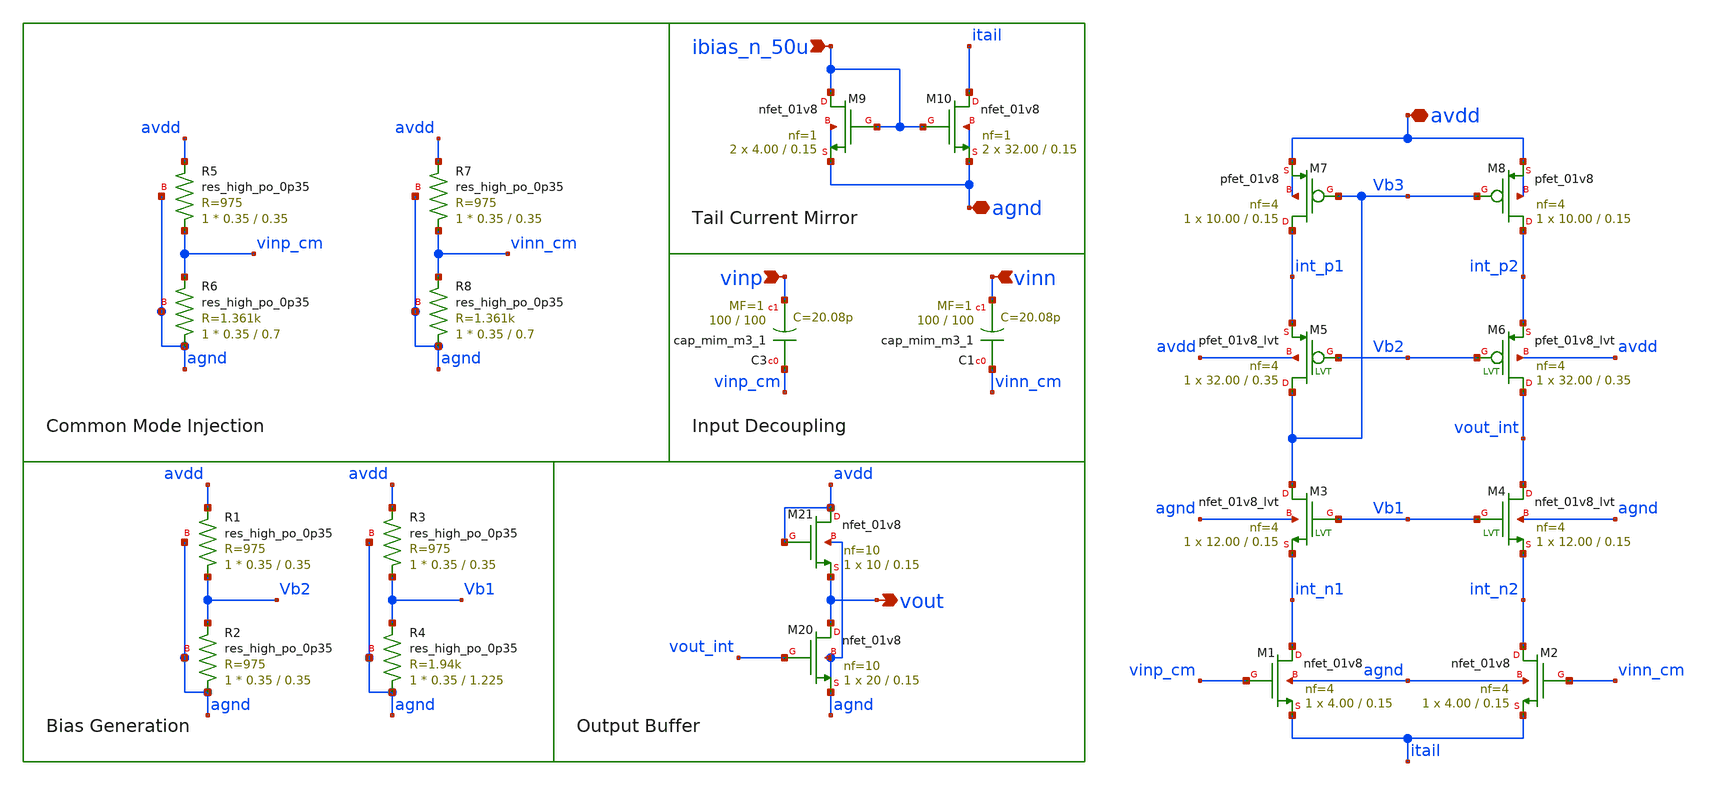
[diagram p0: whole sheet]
** sch_path: AMP/Final_Cascode_Simplfied.sch
**.subckt Final_Cascode_Simplfied avdd vinp vout agnd vinn ibias_n_50u
*.iopin avdd
*.ipin vinp
*.opin vout
*.iopin agnd
*.ipin vinn
*.ipin ibias_n_50u
XM1 int_n1 vinp_cm itail agnd sky130_fd_pr__nfet_01v8 L=0.15 W=4.00 nf=4 ad='int((nf+1)/2) * W/nf * 0.29'
+ as='int((nf+2)/2) * W/nf * 0.29' pd='2*int((nf+1)/2) * (W/nf + 0.29)' ps='2*int((nf+2)/2) * (W/nf + 0.29)'
+ nrd='0.29 / W' nrs='0.29 / W' sa=0 sb=0 sd=0 mult=1 m=1
XM2 int_n2 vinn_cm itail agnd sky130_fd_pr__nfet_01v8 L=0.15 W=4.00 nf=4 ad='int((nf+1)/2) * W/nf * 0.29'
+ as='int((nf+2)/2) * W/nf * 0.29' pd='2*int((nf+1)/2) * (W/nf + 0.29)' ps='2*int((nf+2)/2) * (W/nf + 0.29)'
+ nrd='0.29 / W' nrs='0.29 / W' sa=0 sb=0 sd=0 mult=1 m=1
XM7 int_p1 Vb3 avdd avdd sky130_fd_pr__pfet_01v8 L=0.15 W=10.00 nf=4 ad='int((nf+1)/2) * W/nf * 0.29'
+ as='int((nf+2)/2) * W/nf * 0.29' pd='2*int((nf+1)/2) * (W/nf + 0.29)' ps='2*int((nf+2)/2) * (W/nf + 0.29)'
+ nrd='0.29 / W' nrs='0.29 / W' sa=0 sb=0 sd=0 mult=1 m=1
XM8 int_p2 Vb3 avdd avdd sky130_fd_pr__pfet_01v8 L=0.15 W=10.00 nf=4 ad='int((nf+1)/2) * W/nf * 0.29'
+ as='int((nf+2)/2) * W/nf * 0.29' pd='2*int((nf+1)/2) * (W/nf + 0.29)' ps='2*int((nf+2)/2) * (W/nf + 0.29)'
+ nrd='0.29 / W' nrs='0.29 / W' sa=0 sb=0 sd=0 mult=1 m=1
XM9 ibias_n_50u ibias_n_50u agnd agnd sky130_fd_pr__nfet_01v8 L=0.15 W=4.00 nf=1 ad='int((nf+1)/2) * W/nf * 0.29'
+ as='int((nf+2)/2) * W/nf * 0.29' pd='2*int((nf+1)/2) * (W/nf + 0.29)' ps='2*int((nf+2)/2) * (W/nf + 0.29)'
+ nrd='0.29 / W' nrs='0.29 / W' sa=0 sb=0 sd=0 mult=2 m=2
XM10 itail ibias_n_50u agnd agnd sky130_fd_pr__nfet_01v8 L=0.15 W=32.00 nf=1 ad='int((nf+1)/2) * W/nf * 0.29'
+ as='int((nf+2)/2) * W/nf * 0.29' pd='2*int((nf+1)/2) * (W/nf + 0.29)' ps='2*int((nf+2)/2) * (W/nf + 0.29)'
+ nrd='0.29 / W' nrs='0.29 / W' sa=0 sb=0 sd=0 mult=2 m=2
XM3 Vb3 Vb1 int_n1 agnd sky130_fd_pr__nfet_01v8_lvt L=0.15 W=12.00 nf=4 ad='int((nf+1)/2) * W/nf * 0.29'
+ as='int((nf+2)/2) * W/nf * 0.29' pd='2*int((nf+1)/2) * (W/nf + 0.29)' ps='2*int((nf+2)/2) * (W/nf + 0.29)'
+ nrd='0.29 / W' nrs='0.29 / W' sa=0 sb=0 sd=0 mult=1 m=1
XM4 vout_int Vb1 int_n2 agnd sky130_fd_pr__nfet_01v8_lvt L=0.15 W=12.00 nf=4 ad='int((nf+1)/2) * W/nf * 0.29'
+ as='int((nf+2)/2) * W/nf * 0.29' pd='2*int((nf+1)/2) * (W/nf + 0.29)' ps='2*int((nf+2)/2) * (W/nf + 0.29)'
+ nrd='0.29 / W' nrs='0.29 / W' sa=0 sb=0 sd=0 mult=1 m=1
XM5 Vb3 Vb2 int_p1 avdd sky130_fd_pr__pfet_01v8_lvt L=0.35 W=32.00 nf=4 ad='int((nf+1)/2) * W/nf * 0.29'
+ as='int((nf+2)/2) * W/nf * 0.29' pd='2*int((nf+1)/2) * (W/nf + 0.29)' ps='2*int((nf+2)/2) * (W/nf + 0.29)'
+ nrd='0.29 / W' nrs='0.29 / W' sa=0 sb=0 sd=0 mult=1 m=1
XM6 vout_int Vb2 int_p2 avdd sky130_fd_pr__pfet_01v8_lvt L=0.35 W=32.00 nf=4 ad='int((nf+1)/2) * W/nf * 0.29'
+ as='int((nf+2)/2) * W/nf * 0.29' pd='2*int((nf+1)/2) * (W/nf + 0.29)' ps='2*int((nf+2)/2) * (W/nf + 0.29)'
+ nrd='0.29 / W' nrs='0.29 / W' sa=0 sb=0 sd=0 mult=1 m=1
XC3 vinp_cm vinp sky130_fd_pr__cap_mim_m3_1 W=100 L=100 MF=1 m=1
XC1 vinn_cm vinn sky130_fd_pr__cap_mim_m3_1 W=100 L=100 MF=1 m=1
XM20 vout vout_int agnd agnd sky130_fd_pr__nfet_01v8 L=0.15 W=20 nf=10 ad='int((nf+1)/2) * W/nf * 0.29'
+ as='int((nf+2)/2) * W/nf * 0.29' pd='2*int((nf+1)/2) * (W/nf + 0.29)' ps='2*int((nf+2)/2) * (W/nf + 0.29)'
+ nrd='0.29 / W' nrs='0.29 / W' sa=0 sb=0 sd=0 mult=1 m=1
XM21 avdd avdd vout agnd sky130_fd_pr__nfet_01v8 L=0.15 W=10 nf=10 ad='int((nf+1)/2) * W/nf * 0.29' as='int((nf+2)/2) * W/nf * 0.29'
+ pd='2*int((nf+1)/2) * (W/nf + 0.29)' ps='2*int((nf+2)/2) * (W/nf + 0.29)' nrd='0.29 / W' nrs='0.29 / W'
+ sa=0 sb=0 sd=0 mult=1 m=1
XR1 Vb2 avdd agnd sky130_fd_pr__res_high_po_0p35 L=0.35 mult=1 m=1
XR2 agnd Vb2 agnd sky130_fd_pr__res_high_po_0p35 L=0.35 mult=1 m=1
XR3 Vb1 avdd agnd sky130_fd_pr__res_high_po_0p35 L=0.35 mult=1 m=1
XR4 agnd Vb1 agnd sky130_fd_pr__res_high_po_0p35 L=1.225 mult=1 m=1
XR5 vinp_cm avdd agnd sky130_fd_pr__res_high_po_0p35 L=0.35 mult=1 m=1
XR6 agnd vinp_cm agnd sky130_fd_pr__res_high_po_0p35 L=0.7 mult=1 m=1
XR7 vinn_cm avdd agnd sky130_fd_pr__res_high_po_0p35 L=0.35 mult=1 m=1
XR8 agnd vinn_cm agnd sky130_fd_pr__res_high_po_0p35 L=0.7 mult=1 m=1
**.ends
.end
